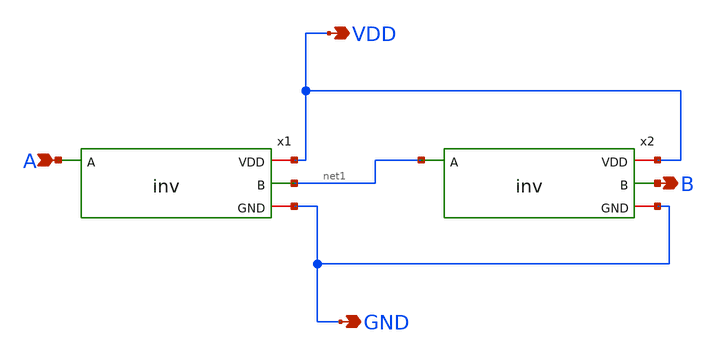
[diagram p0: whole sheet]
** sch_path: designs/libs/tb_analog/tb_buffer/buffer.sch
**.subckt buffer A VDD GND B
*.ipin A
*.opin VDD
*.opin GND
*.opin B
x1 VDD A net1 GND inv
x2 VDD net1 B GND inv
**.ends

* expanding   symbol:  inv.sym # of pins=4
** sym_path: designs/libs/tb_analog/tb_inv/inv.sym
** sch_path: designs/libs/tb_analog/tb_inv/inv.sch
.subckt inv VDD A B GND
*.ipin A
*.opin B
*.iopin VDD
*.iopin GND
XM1 B A GND GND nfet_05v0 L=0.70u W=2u nf=1 ad='int((nf+1)/2) * W/nf * 0.18u' as='int((nf+2)/2) * W/nf * 0.18u'
+ pd='2*int((nf+1)/2) * (W/nf + 0.18u)' ps='2*int((nf+2)/2) * (W/nf + 0.18u)' nrd='0.18u / W' nrs='0.18u / W'
+ sa=0 sb=0 sd=0 m=1
XM2 B A VDD VDD pfet_05v0 L=0.7u W=5u nf=1 ad='int((nf+1)/2) * W/nf * 0.18u' as='int((nf+2)/2) * W/nf * 0.18u'
+ pd='2*int((nf+1)/2) * (W/nf + 0.18u)' ps='2*int((nf+2)/2) * (W/nf + 0.18u)' nrd='0.18u / W' nrs='0.18u / W'
+ sa=0 sb=0 sd=0 m=1
.ends

.end
